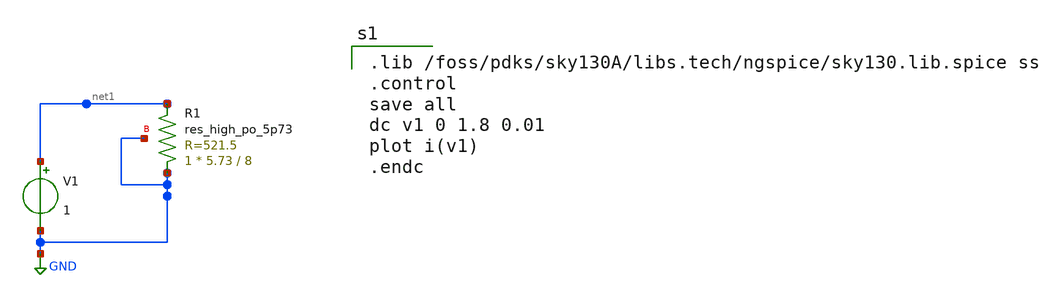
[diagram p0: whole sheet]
** sch_path: res_poly_corners.sch
**.subckt res_poly_corners
V1 net1 GND 1
XR1 GND net1 GND sky130_fd_pr__res_high_po_5p73 L=8 mult=1 m=1
**** begin user architecture code

.lib /foss/pdks/sky130A/libs.tech/ngspice/sky130.lib.spice ss
.control
save all
dc v1 0 1.8 0.01
plot i(v1)
.endc


**** end user architecture code
**.ends
.GLOBAL GND
.end
